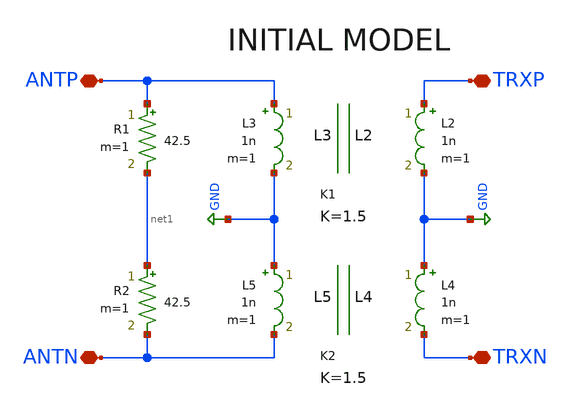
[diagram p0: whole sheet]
** sch_path: mWATTBAT/design_data/xschem/TRX.sch
**.subckt TRX ANTP ANTN TRXP TRXN
*.iopin ANTP
*.iopin ANTN
*.iopin TRXP
*.iopin TRXN
K1 L3 L2 1.5
L2 TRXP GND 1n m=1
L3 ANTP GND 1n m=1
K2 L5 L4 1.5
L4 GND TRXN 1n m=1
L5 GND ANTN 1n m=1
R1 ANTP net1 42.5 m=1
R2 net1 ANTN 42.5 m=1
**.ends
.GLOBAL GND
.end
